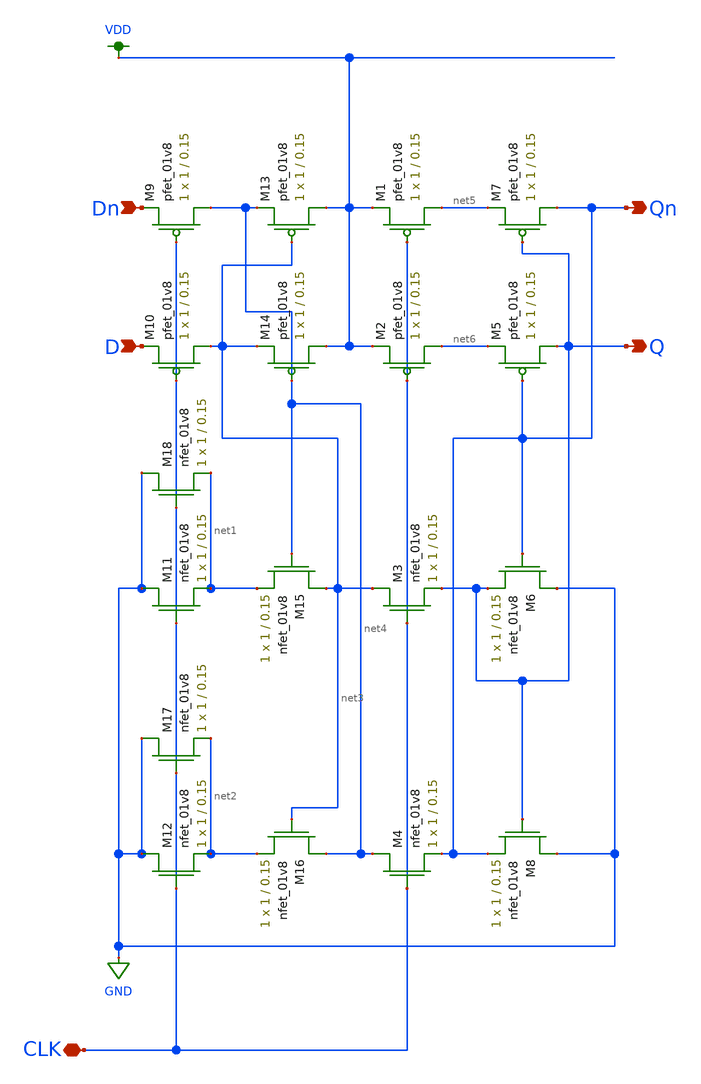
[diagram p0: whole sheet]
** sch_path: schematic/CSRL_D_FF_LVS.sch
**.subckt CSRL_D_FF_LVS Dn D CLK Qn Q
*.ipin Dn
*.ipin D
*.iopin CLK
*.opin Qn
*.opin Q
XM1 net5 CLK VDD VDD sky130_fd_pr__pfet_01v8 L=0.15 W=1 nf=1 ad='int((nf+1)/2) * W/nf * 0.29' as='int((nf+2)/2) * W/nf * 0.29'
+ pd='2*int((nf+1)/2) * (W/nf + 0.29)' ps='2*int((nf+2)/2) * (W/nf + 0.29)' nrd='0.29 / W' nrs='0.29 / W'
+ sa=0 sb=0 sd=0 mult=1 m=1
XM2 net6 CLK VDD VDD sky130_fd_pr__pfet_01v8 L=0.15 W=1 nf=1 ad='int((nf+1)/2) * W/nf * 0.29' as='int((nf+2)/2) * W/nf * 0.29'
+ pd='2*int((nf+1)/2) * (W/nf + 0.29)' ps='2*int((nf+2)/2) * (W/nf + 0.29)' nrd='0.29 / W' nrs='0.29 / W'
+ sa=0 sb=0 sd=0 mult=1 m=1
XM3 net3 CLK Q GND sky130_fd_pr__nfet_01v8 L=0.15 W=1 nf=1 ad='int((nf+1)/2) * W/nf * 0.29' as='int((nf+2)/2) * W/nf * 0.29'
+ pd='2*int((nf+1)/2) * (W/nf + 0.29)' ps='2*int((nf+2)/2) * (W/nf + 0.29)' nrd='0.29 / W' nrs='0.29 / W'
+ sa=0 sb=0 sd=0 mult=1 m=1
XM4 net4 CLK Qn GND sky130_fd_pr__nfet_01v8 L=0.15 W=1 nf=1 ad='int((nf+1)/2) * W/nf * 0.29' as='int((nf+2)/2) * W/nf * 0.29'
+ pd='2*int((nf+1)/2) * (W/nf + 0.29)' ps='2*int((nf+2)/2) * (W/nf + 0.29)' nrd='0.29 / W' nrs='0.29 / W'
+ sa=0 sb=0 sd=0 mult=1 m=1
XM5 Q Qn net6 VDD sky130_fd_pr__pfet_01v8 L=0.15 W=1 nf=1 ad='int((nf+1)/2) * W/nf * 0.29' as='int((nf+2)/2) * W/nf * 0.29'
+ pd='2*int((nf+1)/2) * (W/nf + 0.29)' ps='2*int((nf+2)/2) * (W/nf + 0.29)' nrd='0.29 / W' nrs='0.29 / W'
+ sa=0 sb=0 sd=0 mult=1 m=1
XM6 GND Qn Q GND sky130_fd_pr__nfet_01v8 L=0.15 W=1 nf=1 ad='int((nf+1)/2) * W/nf * 0.29' as='int((nf+2)/2) * W/nf * 0.29'
+ pd='2*int((nf+1)/2) * (W/nf + 0.29)' ps='2*int((nf+2)/2) * (W/nf + 0.29)' nrd='0.29 / W' nrs='0.29 / W'
+ sa=0 sb=0 sd=0 mult=1 m=1
XM7 Qn Q net5 VDD sky130_fd_pr__pfet_01v8 L=0.15 W=1 nf=1 ad='int((nf+1)/2) * W/nf * 0.29' as='int((nf+2)/2) * W/nf * 0.29'
+ pd='2*int((nf+1)/2) * (W/nf + 0.29)' ps='2*int((nf+2)/2) * (W/nf + 0.29)' nrd='0.29 / W' nrs='0.29 / W'
+ sa=0 sb=0 sd=0 mult=1 m=1
XM8 GND Q Qn GND sky130_fd_pr__nfet_01v8 L=0.15 W=1 nf=1 ad='int((nf+1)/2) * W/nf * 0.29' as='int((nf+2)/2) * W/nf * 0.29'
+ pd='2*int((nf+1)/2) * (W/nf + 0.29)' ps='2*int((nf+2)/2) * (W/nf + 0.29)' nrd='0.29 / W' nrs='0.29 / W'
+ sa=0 sb=0 sd=0 mult=1 m=1
XM9 net4 CLK Dn VDD sky130_fd_pr__pfet_01v8 L=0.15 W=1 nf=1 ad='int((nf+1)/2) * W/nf * 0.29' as='int((nf+2)/2) * W/nf * 0.29'
+ pd='2*int((nf+1)/2) * (W/nf + 0.29)' ps='2*int((nf+2)/2) * (W/nf + 0.29)' nrd='0.29 / W' nrs='0.29 / W'
+ sa=0 sb=0 sd=0 mult=1 m=1
XM10 net3 CLK D VDD sky130_fd_pr__pfet_01v8 L=0.15 W=1 nf=1 ad='int((nf+1)/2) * W/nf * 0.29' as='int((nf+2)/2) * W/nf * 0.29'
+ pd='2*int((nf+1)/2) * (W/nf + 0.29)' ps='2*int((nf+2)/2) * (W/nf + 0.29)' nrd='0.29 / W' nrs='0.29 / W'
+ sa=0 sb=0 sd=0 mult=1 m=1
XM11 GND CLK net1 GND sky130_fd_pr__nfet_01v8 L=0.15 W=1 nf=1 ad='int((nf+1)/2) * W/nf * 0.29' as='int((nf+2)/2) * W/nf * 0.29'
+ pd='2*int((nf+1)/2) * (W/nf + 0.29)' ps='2*int((nf+2)/2) * (W/nf + 0.29)' nrd='0.29 / W' nrs='0.29 / W'
+ sa=0 sb=0 sd=0 mult=1 m=1
XM12 GND CLK net2 GND sky130_fd_pr__nfet_01v8 L=0.15 W=1 nf=1 ad='int((nf+1)/2) * W/nf * 0.29' as='int((nf+2)/2) * W/nf * 0.29'
+ pd='2*int((nf+1)/2) * (W/nf + 0.29)' ps='2*int((nf+2)/2) * (W/nf + 0.29)' nrd='0.29 / W' nrs='0.29 / W'
+ sa=0 sb=0 sd=0 mult=1 m=1
XM13 VDD net3 net4 VDD sky130_fd_pr__pfet_01v8 L=0.15 W=1 nf=1 ad='int((nf+1)/2) * W/nf * 0.29' as='int((nf+2)/2) * W/nf * 0.29'
+ pd='2*int((nf+1)/2) * (W/nf + 0.29)' ps='2*int((nf+2)/2) * (W/nf + 0.29)' nrd='0.29 / W' nrs='0.29 / W'
+ sa=0 sb=0 sd=0 mult=1 m=1
XM14 VDD net4 net3 VDD sky130_fd_pr__pfet_01v8 L=0.15 W=1 nf=1 ad='int((nf+1)/2) * W/nf * 0.29' as='int((nf+2)/2) * W/nf * 0.29'
+ pd='2*int((nf+1)/2) * (W/nf + 0.29)' ps='2*int((nf+2)/2) * (W/nf + 0.29)' nrd='0.29 / W' nrs='0.29 / W'
+ sa=0 sb=0 sd=0 mult=1 m=1
XM15 net3 net4 net1 GND sky130_fd_pr__nfet_01v8 L=0.15 W=1 nf=1 ad='int((nf+1)/2) * W/nf * 0.29' as='int((nf+2)/2) * W/nf * 0.29'
+ pd='2*int((nf+1)/2) * (W/nf + 0.29)' ps='2*int((nf+2)/2) * (W/nf + 0.29)' nrd='0.29 / W' nrs='0.29 / W'
+ sa=0 sb=0 sd=0 mult=1 m=1
XM16 net4 net3 net2 GND sky130_fd_pr__nfet_01v8 L=0.15 W=1 nf=1 ad='int((nf+1)/2) * W/nf * 0.29' as='int((nf+2)/2) * W/nf * 0.29'
+ pd='2*int((nf+1)/2) * (W/nf + 0.29)' ps='2*int((nf+2)/2) * (W/nf + 0.29)' nrd='0.29 / W' nrs='0.29 / W'
+ sa=0 sb=0 sd=0 mult=1 m=1
XM17 GND CLK net2 GND sky130_fd_pr__nfet_01v8 L=0.15 W=1 nf=1 ad='int((nf+1)/2) * W/nf * 0.29' as='int((nf+2)/2) * W/nf * 0.29'
+ pd='2*int((nf+1)/2) * (W/nf + 0.29)' ps='2*int((nf+2)/2) * (W/nf + 0.29)' nrd='0.29 / W' nrs='0.29 / W'
+ sa=0 sb=0 sd=0 mult=1 m=1
XM18 GND CLK net1 GND sky130_fd_pr__nfet_01v8 L=0.15 W=1 nf=1 ad='int((nf+1)/2) * W/nf * 0.29' as='int((nf+2)/2) * W/nf * 0.29'
+ pd='2*int((nf+1)/2) * (W/nf + 0.29)' ps='2*int((nf+2)/2) * (W/nf + 0.29)' nrd='0.29 / W' nrs='0.29 / W'
+ sa=0 sb=0 sd=0 mult=1 m=1
**.ends
.GLOBAL VDD
.GLOBAL GND
.end
